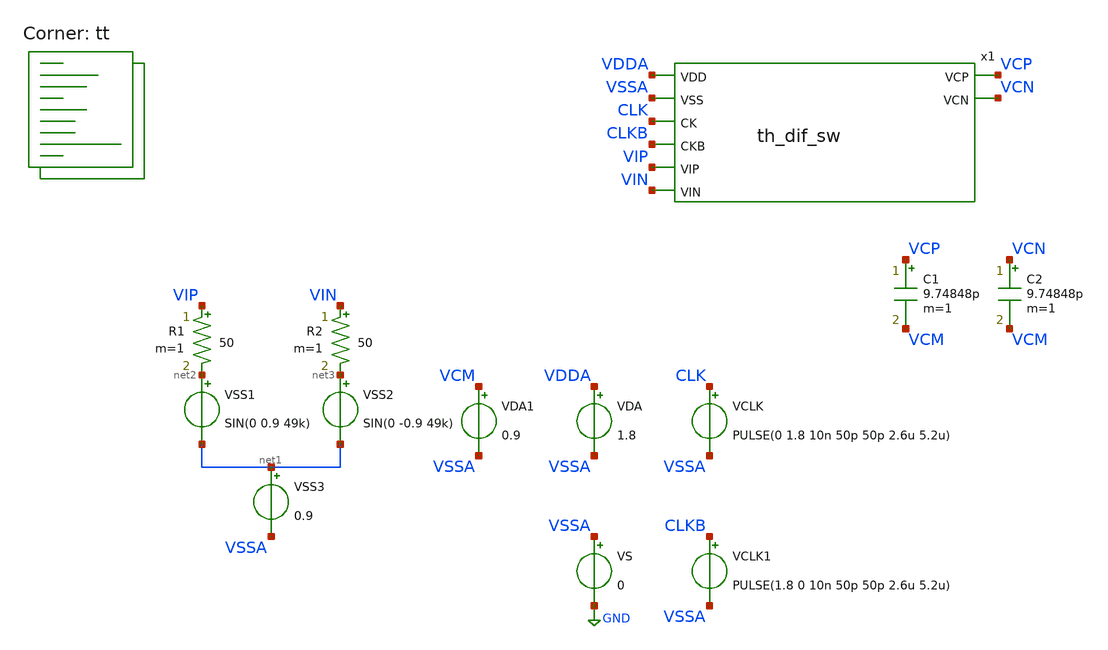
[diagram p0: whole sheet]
** sch_path: xschem/th_sw_tb.sch
**.subckt th_sw_tb
VS VSSA GND 0
VDA VDDA VSSA 1.8
VSS1 net2 net1 SIN(0 0.9 49k)
VSS2 net3 net1 SIN(0 -0.9 49k)
VSS3 net1 VSSA 0.9
VCLK CLK VSSA PULSE(0 1.8 10n 50p 50p 2.6u 5.2u)
R1 VIP net2 50 m=1
R2 VIN net3 50 m=1
x1 VDDA VSSA CLK CLKB VIP VIN VCP VCN th_dif_sw
VCLK1 CLKB VSSA PULSE(1.8 0 10n 50p 50p 2.6u 5.2u)
C1 VCP VCM 9.74848p m=1
C2 VCN VCM 9.74848p m=1
VDA1 VCM VSSA 0.9
**** begin user architecture code

** opencircuitdesign pdks install
* .lib $::SKYWATER_MODELS/sky130.lib.spice tt
.include $PDK_ROOT/$PDK/libs.ref/sky130_fd_sc_hs/spice/sky130_fd_sc_hs.spice



.option wnflag=0
.option savecurrents
.options method=trapezoid
.options solver=iterative
.control
global netlist_dir .
set wr_singlescale
save all
tran 10n 2m  ; Mengubah start time menjadi 1n
remzerovec
write th_sw_tb.raw
exit 1
.endc

.lib $::SKYWATER_MODELS/sky130.lib.spice tt
**** end user architecture code
**.ends
.GLOBAL GND
.end
